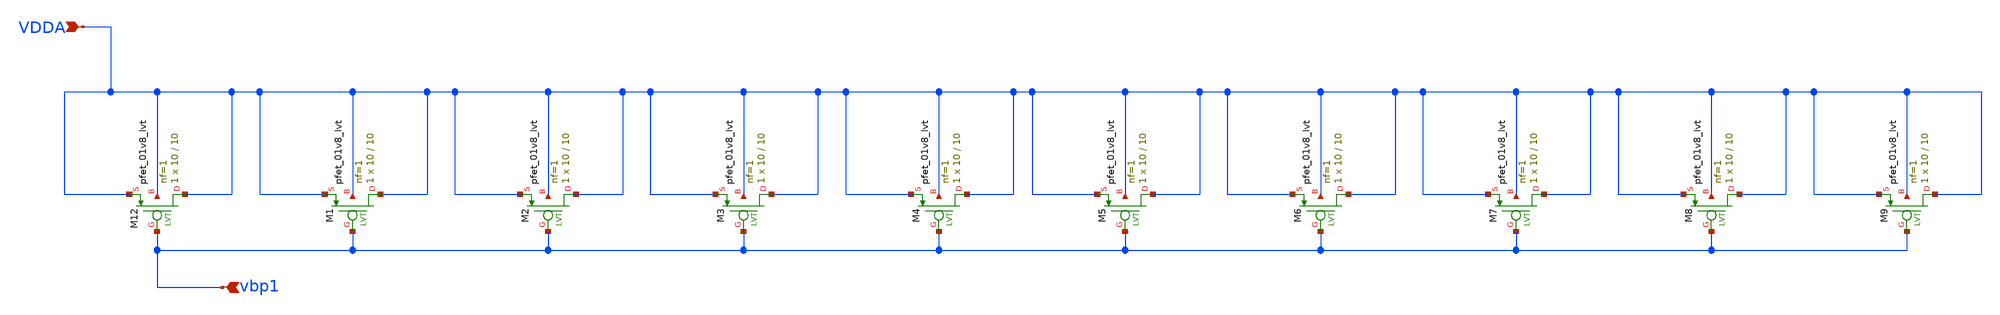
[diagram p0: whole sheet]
** sch_path: lef/lef/gds/bg2_decoupling_cap.sch
**.subckt bg2_decoupling_cap VDDA vbp1
*.ipin VDDA
*.ipin vbp1
XM12 VDDA vbp1 VDDA VDDA sky130_fd_pr__pfet_01v8_lvt L=10 W=10 nf=1 ad='int((1 + 1)/2) * 10 / 1 * 0.29'
+ as='int((1 + 2)/2) * 10 / 1 * 0.29' pd='2*int((1 + 1)/2) * (10 / 1 + 0.29)' ps='2*int((1 + 2)/2) * (10 / 1 + 0.29)'
+ nrd='0.29 / 10 ' nrs='0.29 / 10 ' sa=0 sb=0 sd=0 mult=1 m=1
XM1 VDDA vbp1 VDDA VDDA sky130_fd_pr__pfet_01v8_lvt L=10 W=10 nf=1 ad='int((1 + 1)/2) * 10 / 1 * 0.29'
+ as='int((1 + 2)/2) * 10 / 1 * 0.29' pd='2*int((1 + 1)/2) * (10 / 1 + 0.29)' ps='2*int((1 + 2)/2) * (10 / 1 + 0.29)'
+ nrd='0.29 / 10 ' nrs='0.29 / 10 ' sa=0 sb=0 sd=0 mult=1 m=1
XM2 VDDA vbp1 VDDA VDDA sky130_fd_pr__pfet_01v8_lvt L=10 W=10 nf=1 ad='int((1 + 1)/2) * 10 / 1 * 0.29'
+ as='int((1 + 2)/2) * 10 / 1 * 0.29' pd='2*int((1 + 1)/2) * (10 / 1 + 0.29)' ps='2*int((1 + 2)/2) * (10 / 1 + 0.29)'
+ nrd='0.29 / 10 ' nrs='0.29 / 10 ' sa=0 sb=0 sd=0 mult=1 m=1
XM3 VDDA vbp1 VDDA VDDA sky130_fd_pr__pfet_01v8_lvt L=10 W=10 nf=1 ad='int((1 + 1)/2) * 10 / 1 * 0.29'
+ as='int((1 + 2)/2) * 10 / 1 * 0.29' pd='2*int((1 + 1)/2) * (10 / 1 + 0.29)' ps='2*int((1 + 2)/2) * (10 / 1 + 0.29)'
+ nrd='0.29 / 10 ' nrs='0.29 / 10 ' sa=0 sb=0 sd=0 mult=1 m=1
XM4 VDDA vbp1 VDDA VDDA sky130_fd_pr__pfet_01v8_lvt L=10 W=10 nf=1 ad='int((1 + 1)/2) * 10 / 1 * 0.29'
+ as='int((1 + 2)/2) * 10 / 1 * 0.29' pd='2*int((1 + 1)/2) * (10 / 1 + 0.29)' ps='2*int((1 + 2)/2) * (10 / 1 + 0.29)'
+ nrd='0.29 / 10 ' nrs='0.29 / 10 ' sa=0 sb=0 sd=0 mult=1 m=1
XM5 VDDA vbp1 VDDA VDDA sky130_fd_pr__pfet_01v8_lvt L=10 W=10 nf=1 ad='int((1 + 1)/2) * 10 / 1 * 0.29'
+ as='int((1 + 2)/2) * 10 / 1 * 0.29' pd='2*int((1 + 1)/2) * (10 / 1 + 0.29)' ps='2*int((1 + 2)/2) * (10 / 1 + 0.29)'
+ nrd='0.29 / 10 ' nrs='0.29 / 10 ' sa=0 sb=0 sd=0 mult=1 m=1
XM6 VDDA vbp1 VDDA VDDA sky130_fd_pr__pfet_01v8_lvt L=10 W=10 nf=1 ad='int((1 + 1)/2) * 10 / 1 * 0.29'
+ as='int((1 + 2)/2) * 10 / 1 * 0.29' pd='2*int((1 + 1)/2) * (10 / 1 + 0.29)' ps='2*int((1 + 2)/2) * (10 / 1 + 0.29)'
+ nrd='0.29 / 10 ' nrs='0.29 / 10 ' sa=0 sb=0 sd=0 mult=1 m=1
XM7 VDDA vbp1 VDDA VDDA sky130_fd_pr__pfet_01v8_lvt L=10 W=10 nf=1 ad='int((1 + 1)/2) * 10 / 1 * 0.29'
+ as='int((1 + 2)/2) * 10 / 1 * 0.29' pd='2*int((1 + 1)/2) * (10 / 1 + 0.29)' ps='2*int((1 + 2)/2) * (10 / 1 + 0.29)'
+ nrd='0.29 / 10 ' nrs='0.29 / 10 ' sa=0 sb=0 sd=0 mult=1 m=1
XM8 VDDA vbp1 VDDA VDDA sky130_fd_pr__pfet_01v8_lvt L=10 W=10 nf=1 ad='int((1 + 1)/2) * 10 / 1 * 0.29'
+ as='int((1 + 2)/2) * 10 / 1 * 0.29' pd='2*int((1 + 1)/2) * (10 / 1 + 0.29)' ps='2*int((1 + 2)/2) * (10 / 1 + 0.29)'
+ nrd='0.29 / 10 ' nrs='0.29 / 10 ' sa=0 sb=0 sd=0 mult=1 m=1
XM9 VDDA vbp1 VDDA VDDA sky130_fd_pr__pfet_01v8_lvt L=10 W=10 nf=1 ad='int((1 + 1)/2) * 10 / 1 * 0.29'
+ as='int((1 + 2)/2) * 10 / 1 * 0.29' pd='2*int((1 + 1)/2) * (10 / 1 + 0.29)' ps='2*int((1 + 2)/2) * (10 / 1 + 0.29)'
+ nrd='0.29 / 10 ' nrs='0.29 / 10 ' sa=0 sb=0 sd=0 mult=1 m=1
**.ends
.end
